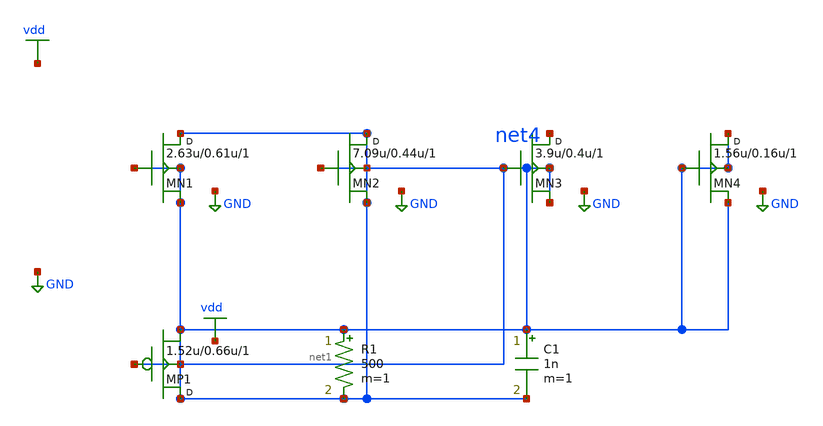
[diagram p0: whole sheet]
** sch_path: synthetic/generated/0044_synthetic.sch
**.subckt 0044_synthetic
MN1 net1 net1 net1 net1 nmos w=2.63u l=0.61u m=1
MN2 net1 net1 net1 net1 nmos w=7.09u l=0.44u m=1
MN3 net4 net1 net1 net1 nmos w=3.9u l=0.4u m=1
MN4 net1 net1 net1 net1 nmos w=1.56u l=0.16u m=1
MP1 net1 net1 net1 net1 pmos w=1.52u l=0.66u m=1
R1 net1 net1 500 m=1
C1 net1 net1 1n m=1
**.ends
.GLOBAL GND
.GLOBAL vdd
.end
